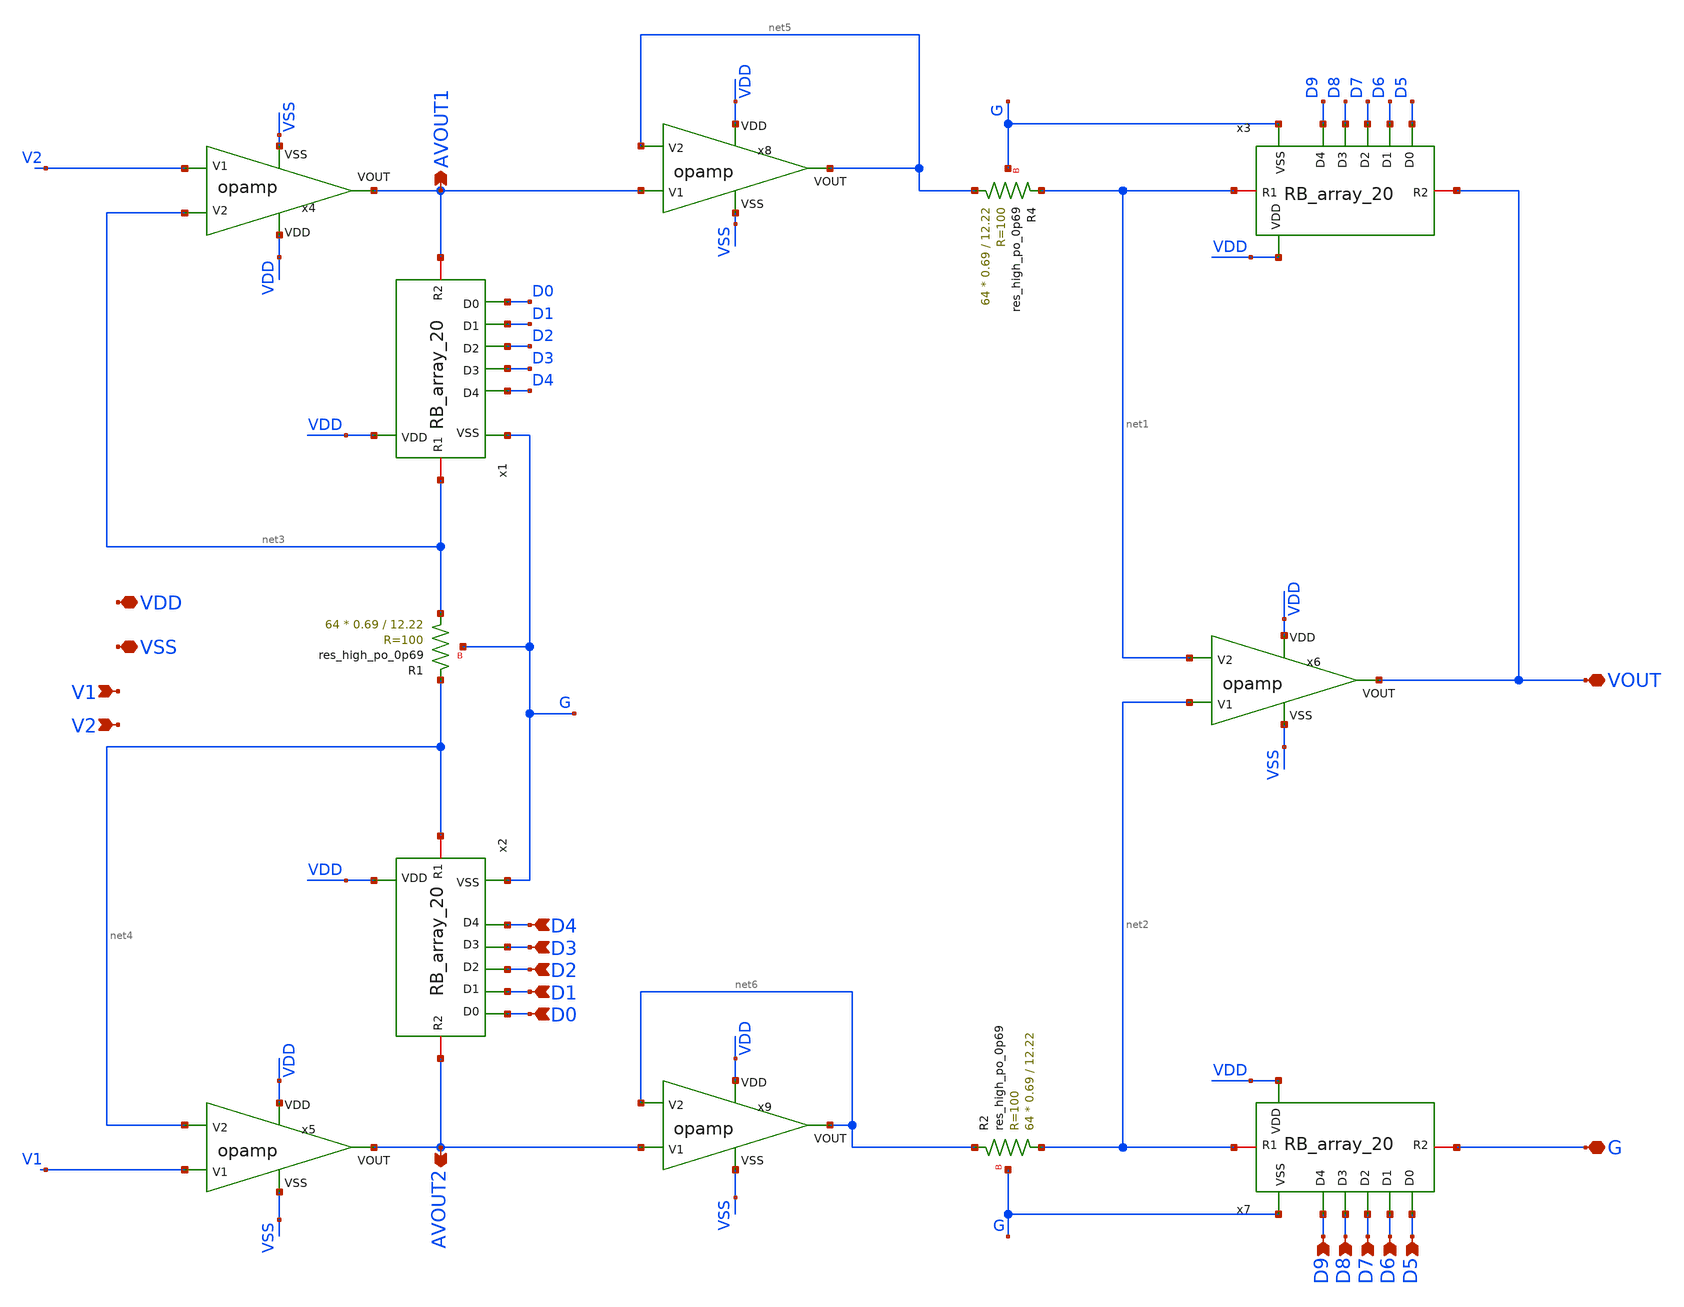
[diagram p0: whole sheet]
** sch_path: xschem/sky130_hcmus_ip__instramp.sch
**.subckt sky130_hcmus_ip__instramp VOUT G VDD VSS V1 V2 D4 D3 D2 D1 D0 D9 D8 D7 D6 D5 AVOUT1 AVOUT2
*.iopin VOUT
*.iopin G
*.iopin VDD
*.iopin VSS
*.ipin V1
*.ipin V2
*.ipin D4
*.ipin D3
*.ipin D2
*.ipin D1
*.ipin D0
*.ipin D9
*.ipin D8
*.ipin D7
*.ipin D6
*.ipin D5
*.opin AVOUT1
*.opin AVOUT2
x4 VDD VSS V2 net3 AVOUT1 opamp
x5 VDD VSS V1 net4 AVOUT2 opamp
x6 VDD VSS net2 net1 VOUT opamp
x1 G net3 AVOUT1 D0 D1 D2 D3 D4 VDD RB_array_20
x2 G net4 AVOUT2 D0 D1 D2 D3 D4 VDD RB_array_20
x3 G net1 VOUT D5 D6 D7 D8 D9 VDD RB_array_20
x7 G net2 G D5 D6 D7 D8 D9 VDD RB_array_20
XR4 net5 net1 G sky130_fd_pr__res_high_po_0p69 L=12.22 mult=64 m=64
XR1 net3 net4 G sky130_fd_pr__res_high_po_0p69 L=12.22 mult=64 m=64
XR2 net2 net6 G sky130_fd_pr__res_high_po_0p69 L=12.22 mult=64 m=64
x8 VDD VSS AVOUT1 net5 net5 opamp
x9 VDD VSS AVOUT2 net6 net6 opamp
**.ends

* expanding   symbol:  ../xschem/opamp.sym # of pins=5
** sym_path: xschem/opamp.sym
** sch_path: xschem/opamp.sch
.subckt opamp VDD VSS V1 V2 VOUT
*.ipin VSS
*.ipin VDD
*.ipin V2
*.ipin V1
*.opin VOUT
XM2 net5 V2 net1 VSS sky130_fd_pr__nfet_01v8 L=1 W=8.5 nf=1 ad='int((nf+1)/2) * W/nf * 0.29' as='int((nf+2)/2) * W/nf * 0.29'
+ pd='2*int((nf+1)/2) * (W/nf + 0.29)' ps='2*int((nf+2)/2) * (W/nf + 0.29)' nrd='0.29 / W' nrs='0.29 / W'
+ sa=0 sb=0 sd=0 mult=1 m=1
XM1 net6 net5 VDD VDD sky130_fd_pr__pfet_01v8 L=1 W=41 nf=1 ad='int((nf+1)/2) * W/nf * 0.29' as='int((nf+2)/2) * W/nf * 0.29'
+ pd='2*int((nf+1)/2) * (W/nf + 0.29)' ps='2*int((nf+2)/2) * (W/nf + 0.29)' nrd='0.29 / W' nrs='0.29 / W'
+ sa=0 sb=0 sd=0 mult=1 m=1
XM4 net6 V1 net1 VSS sky130_fd_pr__nfet_01v8 L=1 W=8.5 nf=1 ad='int((nf+1)/2) * W/nf * 0.29' as='int((nf+2)/2) * W/nf * 0.29'
+ pd='2*int((nf+1)/2) * (W/nf + 0.29)' ps='2*int((nf+2)/2) * (W/nf + 0.29)' nrd='0.29 / W' nrs='0.29 / W'
+ sa=0 sb=0 sd=0 mult=1 m=1
XM5 net1 net4 VSS VSS sky130_fd_pr__nfet_01v8 L=1 W=20 nf=1 ad='int((nf+1)/2) * W/nf * 0.29' as='int((nf+2)/2) * W/nf * 0.29'
+ pd='2*int((nf+1)/2) * (W/nf + 0.29)' ps='2*int((nf+2)/2) * (W/nf + 0.29)' nrd='0.29 / W' nrs='0.29 / W'
+ sa=0 sb=0 sd=0 mult=1 m=1
XM6 VOUT net4 VSS VSS sky130_fd_pr__nfet_01v8 L=1 W=19 nf=1 ad='int((nf+1)/2) * W/nf * 0.29' as='int((nf+2)/2) * W/nf * 0.29'
+ pd='2*int((nf+1)/2) * (W/nf + 0.29)' ps='2*int((nf+2)/2) * (W/nf + 0.29)' nrd='0.29 / W' nrs='0.29 / W'
+ sa=0 sb=0 sd=0 mult=1 m=1
XM7 net4 net4 VSS VSS sky130_fd_pr__nfet_01v8 L=1 W=20 nf=1 ad='int((nf+1)/2) * W/nf * 0.29' as='int((nf+2)/2) * W/nf * 0.29'
+ pd='2*int((nf+1)/2) * (W/nf + 0.29)' ps='2*int((nf+2)/2) * (W/nf + 0.29)' nrd='0.29 / W' nrs='0.29 / W'
+ sa=0 sb=0 sd=0 mult=1 m=1
XM3 net5 net5 VDD VDD sky130_fd_pr__pfet_01v8 L=1 W=41 nf=1 ad='int((nf+1)/2) * W/nf * 0.29' as='int((nf+2)/2) * W/nf * 0.29'
+ pd='2*int((nf+1)/2) * (W/nf + 0.29)' ps='2*int((nf+2)/2) * (W/nf + 0.29)' nrd='0.29 / W' nrs='0.29 / W'
+ sa=0 sb=0 sd=0 mult=1 m=1
XM8 VOUT net6 VDD VDD sky130_fd_pr__pfet_01v8 L=1 W=40 nf=1 ad='int((nf+1)/2) * W/nf * 0.29' as='int((nf+2)/2) * W/nf * 0.29'
+ pd='2*int((nf+1)/2) * (W/nf + 0.29)' ps='2*int((nf+2)/2) * (W/nf + 0.29)' nrd='0.29 / W' nrs='0.29 / W'
+ sa=0 sb=0 sd=0 mult=2 m=2
XR3 net2 VDD VSS sky130_fd_pr__res_high_po W=1 L=50 mult=1 m=1
XR1 net3 net2 VSS sky130_fd_pr__res_high_po W=1 L=50 mult=1 m=1
XR2 net4 net3 VSS sky130_fd_pr__res_high_po W=1 L=50 mult=1 m=1
XR4 net7 VOUT VSS sky130_fd_pr__res_high_po W=1 L=7 mult=1 m=1
XC1 net7 net6 sky130_fd_pr__cap_mim_m3_1 W=5.55 L=10 MF=20 m=20
.ends


* expanding   symbol:  ../xschem/RB_array_20.sym # of pins=9
** sym_path: xschem/RB_array_20.sym
** sch_path: xschem/RB_array_20.sch
.subckt RB_array_20 VSS R1 R2 D0 D1 D2 D3 D4 VDD
*.ipin VSS
*.iopin R2
*.ipin D0
*.ipin D1
*.ipin D2
*.ipin D3
*.ipin D4
*.iopin R1
*.ipin VDD
XR2 net6 R2 VSS sky130_fd_pr__res_high_po_0p69 L=12.22 mult=1 m=1
XR1 net1 R2 VSS sky130_fd_pr__res_high_po_0p69 L=12.22 mult=1 m=1
XR3 net5 R2 VSS sky130_fd_pr__res_high_po_0p69 L=12.22 mult=2 m=2
XR4 net4 R2 VSS sky130_fd_pr__res_high_po_0p69 L=12.22 mult=4 m=4
XR5 net3 R2 VSS sky130_fd_pr__res_high_po_0p69 L=12.22 mult=8 m=8
XR6 net2 R2 VSS sky130_fd_pr__res_high_po_0p69 L=12.22 mult=16 m=16
XM6 net8 D0 net1 VSS sky130_fd_pr__nfet_g5v0d10v5 L=1 W=4.77 nf=1 ad='int((nf+1)/2) * W/nf * 0.29' as='int((nf+2)/2) * W/nf * 0.29'
+ pd='2*int((nf+1)/2) * (W/nf + 0.29)' ps='2*int((nf+2)/2) * (W/nf + 0.29)' nrd='0.29 / W' nrs='0.29 / W'
+ sa=0 sb=0 sd=0 mult=1 m=1
XM7 net12 D1 net5 VSS sky130_fd_pr__nfet_g5v0d10v5 L=1 W=9.74 nf=2 ad='int((nf+1)/2) * W/nf * 0.29' as='int((nf+2)/2) * W/nf * 0.29'
+ pd='2*int((nf+1)/2) * (W/nf + 0.29)' ps='2*int((nf+2)/2) * (W/nf + 0.29)' nrd='0.29 / W' nrs='0.29 / W'
+ sa=0 sb=0 sd=0 mult=1 m=1
XM8 net9 D2 net4 VSS sky130_fd_pr__nfet_g5v0d10v5 L=1 W=18.60 nf=4 ad='int((nf+1)/2) * W/nf * 0.29' as='int((nf+2)/2) * W/nf * 0.29'
+ pd='2*int((nf+1)/2) * (W/nf + 0.29)' ps='2*int((nf+2)/2) * (W/nf + 0.29)' nrd='0.29 / W' nrs='0.29 / W'
+ sa=0 sb=0 sd=0 mult=1 m=1
XM9 net10 D3 net3 VSS sky130_fd_pr__nfet_g5v0d10v5 L=1 W=35.04 nf=8 ad='int((nf+1)/2) * W/nf * 0.29'
+ as='int((nf+2)/2) * W/nf * 0.29' pd='2*int((nf+1)/2) * (W/nf + 0.29)' ps='2*int((nf+2)/2) * (W/nf + 0.29)'
+ nrd='0.29 / W' nrs='0.29 / W' sa=0 sb=0 sd=0 mult=1 m=1
XM10 net11 D4 net2 VSS sky130_fd_pr__nfet_g5v0d10v5 L=1 W=61.60 nf=14 ad='int((nf+1)/2) * W/nf * 0.29'
+ as='int((nf+2)/2) * W/nf * 0.29' pd='2*int((nf+1)/2) * (W/nf + 0.29)' ps='2*int((nf+2)/2) * (W/nf + 0.29)'
+ nrd='0.29 / W' nrs='0.29 / W' sa=0 sb=0 sd=0 mult=1 m=1
XM11 net7 VDD net6 VSS sky130_fd_pr__nfet_g5v0d10v5 L=1 W=4.77 nf=1 ad='int((nf+1)/2) * W/nf * 0.29'
+ as='int((nf+2)/2) * W/nf * 0.29' pd='2*int((nf+1)/2) * (W/nf + 0.29)' ps='2*int((nf+2)/2) * (W/nf + 0.29)'
+ nrd='0.29 / W' nrs='0.29 / W' sa=0 sb=0 sd=0 mult=1 m=1
Vmeas R1 net7 0
.save i(vmeas)
Vmeas1 R1 net8 0
.save i(vmeas1)
Vmeas2 R1 net12 0
.save i(vmeas2)
Vmeas3 R1 net9 0
.save i(vmeas3)
Vmeas4 R1 net10 0
.save i(vmeas4)
Vmeas5 R1 net11 0
.save i(vmeas5)
.ends

.end
